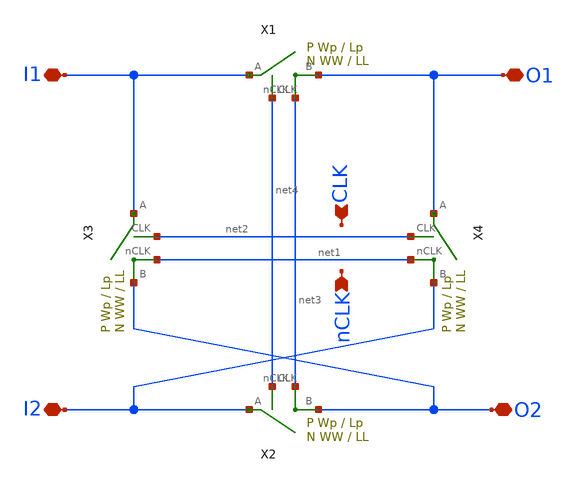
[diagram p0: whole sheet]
** sch_path: schematic/chop2.sch
**.subckt chop2 O2 O1 I2 I1 CLK nCLK
*.iopin O2
*.iopin O1
*.iopin I2
*.iopin I1
*.ipin CLK
*.ipin nCLK
X1 O1 I1 net4 net3 switch Wp=Wp Lp=Lp WW=WW LL=LL
X2 O2 I2 net4 net3 switch Wp=Wp Lp=Lp WW=WW LL=LL
X3 O2 I1 net2 net1 switch Wp=Wp Lp=Lp WW=WW LL=LL
X4 I2 O1 net2 net1 switch Wp=Wp Lp=Lp WW=WW LL=LL
**.ends

* expanding   symbol:  /home/madvlsi/Documents/MADVLSI-Final_Project/schematic/switch.sym # of
*+ pins=4
** sym_path: schematic/switch.sym
** sch_path: schematic/switch.sch
.subckt switch B A CLK nCLK  Wp=1 Lp=0.15 WW=1 LL=0.15
*.iopin B
*.iopin A
*.ipin CLK
*.ipin nCLK
*.ipin CLK
*.ipin CLK
*.ipin nCLK
*.ipin nCLK
XM1 A CLK B GND sky130_fd_pr__nfet_01v8 L={LL} W={WW} nf=1 ad='int((nf+1)/2) * W/nf * 0.29' as='int((nf+2)/2) * W/nf * 0.29'
+ pd='2*int((nf+1)/2) * (W/nf + 0.29)' ps='2*int((nf+2)/2) * (W/nf + 0.29)' nrd='0.29 / W' nrs='0.29 / W'
+ sa=0 sb=0 sd=0 mult=1 m=1
XM2 A nCLK B VDD sky130_fd_pr__pfet_01v8 L={Lp} W={Wp} nf=1 ad='int((nf+1)/2) * W/nf * 0.29' as='int((nf+2)/2) * W/nf * 0.29'
+ pd='2*int((nf+1)/2) * (W/nf + 0.29)' ps='2*int((nf+2)/2) * (W/nf + 0.29)' nrd='0.29 / W' nrs='0.29 / W'
+ sa=0 sb=0 sd=0 mult=1 m=1
XM3 B CLK B VDD sky130_fd_pr__pfet_01v8 L={Lp} W={Wp/2} nf=1 ad='int((nf+1)/2) * W/nf * 0.29' as='int((nf+2)/2) * W/nf * 0.29'
+ pd='2*int((nf+1)/2) * (W/nf + 0.29)' ps='2*int((nf+2)/2) * (W/nf + 0.29)' nrd='0.29 / W' nrs='0.29 / W'
+ sa=0 sb=0 sd=0 mult=1 m=1
XM4 A CLK A VDD sky130_fd_pr__pfet_01v8 L={Lp} W={Wp/2} nf=1 ad='int((nf+1)/2) * W/nf * 0.29' as='int((nf+2)/2) * W/nf * 0.29'
+ pd='2*int((nf+1)/2) * (W/nf + 0.29)' ps='2*int((nf+2)/2) * (W/nf + 0.29)' nrd='0.29 / W' nrs='0.29 / W'
+ sa=0 sb=0 sd=0 mult=1 m=1
XM5 B nCLK B GND sky130_fd_pr__nfet_01v8 L={LL} W={WW/2} nf=1 ad='int((nf+1)/2) * W/nf * 0.29' as='int((nf+2)/2) * W/nf * 0.29'
+ pd='2*int((nf+1)/2) * (W/nf + 0.29)' ps='2*int((nf+2)/2) * (W/nf + 0.29)' nrd='0.29 / W' nrs='0.29 / W'
+ sa=0 sb=0 sd=0 mult=1 m=1
XM6 A nCLK A GND sky130_fd_pr__nfet_01v8 L={LL} W={WW/2} nf=1 ad='int((nf+1)/2) * W/nf * 0.29' as='int((nf+2)/2) * W/nf * 0.29'
+ pd='2*int((nf+1)/2) * (W/nf + 0.29)' ps='2*int((nf+2)/2) * (W/nf + 0.29)' nrd='0.29 / W' nrs='0.29 / W'
+ sa=0 sb=0 sd=0 mult=1 m=1
.ends

.end
